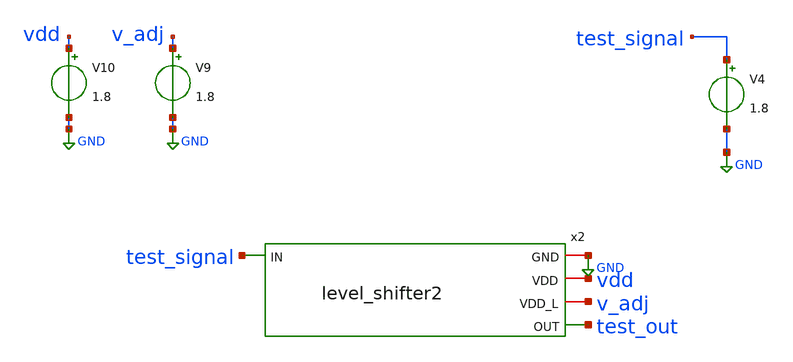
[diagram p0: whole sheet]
** sch_path: xschem/tb_level.sch
**.subckt tb_level
V4 test_signal GND 1.8
V9 v_adj GND 1.8
V10 vdd GND 1.8
x2 GND vdd v_adj test_signal test_out level_shifter2
**** begin user architecture code

** opencircuitdesign pdks install
.lib $::SKYWATER_MODELS/sky130.lib.spice tt




* .options filetype=ascii
.control
  let vstart = 0.6
  let vstop = 0.5
  let vstep = -0.1
  let vcurrent = vstart
  while vcurrent >= vstop
    alter V9 vcurrent
    alter @V4[PULSE] [ 0 $&vcurrent 0 10n 10n 200n 500n ]
    tran 0.05n 1u
    write tb_level.raw
    set appendwrite

    let vcurrent = vcurrent + vstep
  end
.endc

.end


**** end user architecture code
**.ends

* expanding   symbol:  level_shifter2.sym # of pins=5
** sym_path: xschem/level_shifter2.sym
** sch_path: xschem/level_shifter2.sch
.subckt level_shifter2 GND VDD VDD_L IN OUT
*.iopin VDD_L
*.iopin VDD
*.iopin GND
*.ipin IN
*.opin OUT
XM5 out_p src_n net1 VDD sky130_fd_pr__pfet_01v8_hvt L=0.15 W=1.68 nf=1 ad='int((nf+1)/2) * W/nf * 0.29'
+ as='int((nf+2)/2) * W/nf * 0.29' pd='2*int((nf+1)/2) * (W/nf + 0.29)' ps='2*int((nf+2)/2) * (W/nf + 0.29)'
+ nrd='0.29 / W' nrs='0.29 / W' sa=0 sb=0 sd=0 mult=1 m=1
XM6 out_n IN net1 VDD sky130_fd_pr__pfet_01v8_hvt L=0.15 W=1.68 nf=1 ad='int((nf+1)/2) * W/nf * 0.29'
+ as='int((nf+2)/2) * W/nf * 0.29' pd='2*int((nf+1)/2) * (W/nf + 0.29)' ps='2*int((nf+2)/2) * (W/nf + 0.29)'
+ nrd='0.29 / W' nrs='0.29 / W' sa=0 sb=0 sd=0 mult=1 m=1
XM7 out_p out_p GND GND sky130_fd_pr__nfet_01v8 L=0.3 W=0.42 nf=1 ad='int((nf+1)/2) * W/nf * 0.29' as='int((nf+2)/2) * W/nf * 0.29'
+ pd='2*int((nf+1)/2) * (W/nf + 0.29)' ps='2*int((nf+2)/2) * (W/nf + 0.29)' nrd='0.29 / W' nrs='0.29 / W'
+ sa=0 sb=0 sd=0 mult=1 m=1
XM8 out_n out_p GND GND sky130_fd_pr__nfet_01v8 L=0.3 W=0.42 nf=1 ad='int((nf+1)/2) * W/nf * 0.29' as='int((nf+2)/2) * W/nf * 0.29'
+ pd='2*int((nf+1)/2) * (W/nf + 0.29)' ps='2*int((nf+2)/2) * (W/nf + 0.29)' nrd='0.29 / W' nrs='0.29 / W'
+ sa=0 sb=0 sd=0 mult=1 m=1
XM9 OUT out_n GND GND sky130_fd_pr__nfet_01v8 L=0.15 W=0.42 nf=1 ad='int((nf+1)/2) * W/nf * 0.29' as='int((nf+2)/2) * W/nf * 0.29'
+ pd='2*int((nf+1)/2) * (W/nf + 0.29)' ps='2*int((nf+2)/2) * (W/nf + 0.29)' nrd='0.29 / W' nrs='0.29 / W'
+ sa=0 sb=0 sd=0 mult=1 m=1
XM10 OUT out_n VDD VDD sky130_fd_pr__pfet_01v8_hvt L=0.15 W=0.84 nf=1 ad='int((nf+1)/2) * W/nf * 0.29'
+ as='int((nf+2)/2) * W/nf * 0.29' pd='2*int((nf+1)/2) * (W/nf + 0.29)' ps='2*int((nf+2)/2) * (W/nf + 0.29)'
+ nrd='0.29 / W' nrs='0.29 / W' sa=0 sb=0 sd=0 mult=1 m=1
XM1 net1 net2 VDD VDD sky130_fd_pr__pfet_01v8_hvt L=0.3 W=1.68 nf=1 ad='int((nf+1)/2) * W/nf * 0.29'
+ as='int((nf+2)/2) * W/nf * 0.29' pd='2*int((nf+1)/2) * (W/nf + 0.29)' ps='2*int((nf+2)/2) * (W/nf + 0.29)'
+ nrd='0.29 / W' nrs='0.29 / W' sa=0 sb=0 sd=0 mult=1 m=1
XM2 net2 net2 VDD VDD sky130_fd_pr__pfet_01v8_hvt L=0.3 W=0.42 nf=1 ad='int((nf+1)/2) * W/nf * 0.29'
+ as='int((nf+2)/2) * W/nf * 0.29' pd='2*int((nf+1)/2) * (W/nf + 0.29)' ps='2*int((nf+2)/2) * (W/nf + 0.29)'
+ nrd='0.29 / W' nrs='0.29 / W' sa=0 sb=0 sd=0 mult=1 m=1
XM3 net2 net2 GND GND sky130_fd_pr__nfet_01v8 L=0.6 W=0.42 nf=1 ad='int((nf+1)/2) * W/nf * 0.29' as='int((nf+2)/2) * W/nf * 0.29'
+ pd='2*int((nf+1)/2) * (W/nf + 0.29)' ps='2*int((nf+2)/2) * (W/nf + 0.29)' nrd='0.29 / W' nrs='0.29 / W'
+ sa=0 sb=0 sd=0 mult=1 m=1
XM4 src_n src_n VDD_L VDD_L sky130_fd_pr__pfet_01v8_hvt L=0.15 W=0.42 nf=1 ad='int((nf+1)/2) * W/nf * 0.29'
+ as='int((nf+2)/2) * W/nf * 0.29' pd='2*int((nf+1)/2) * (W/nf + 0.29)' ps='2*int((nf+2)/2) * (W/nf + 0.29)'
+ nrd='0.29 / W' nrs='0.29 / W' sa=0 sb=0 sd=0 mult=1 m=1
XM11 src_n src_n GND GND sky130_fd_pr__nfet_01v8 L=0.6 W=0.42 nf=1 ad='int((nf+1)/2) * W/nf * 0.29' as='int((nf+2)/2) * W/nf * 0.29'
+ pd='2*int((nf+1)/2) * (W/nf + 0.29)' ps='2*int((nf+2)/2) * (W/nf + 0.29)' nrd='0.29 / W' nrs='0.29 / W'
+ sa=0 sb=0 sd=0 mult=1 m=1
.ends

.GLOBAL GND
.GLOBAL VDD
.GLOBAL VDD_L
.end
